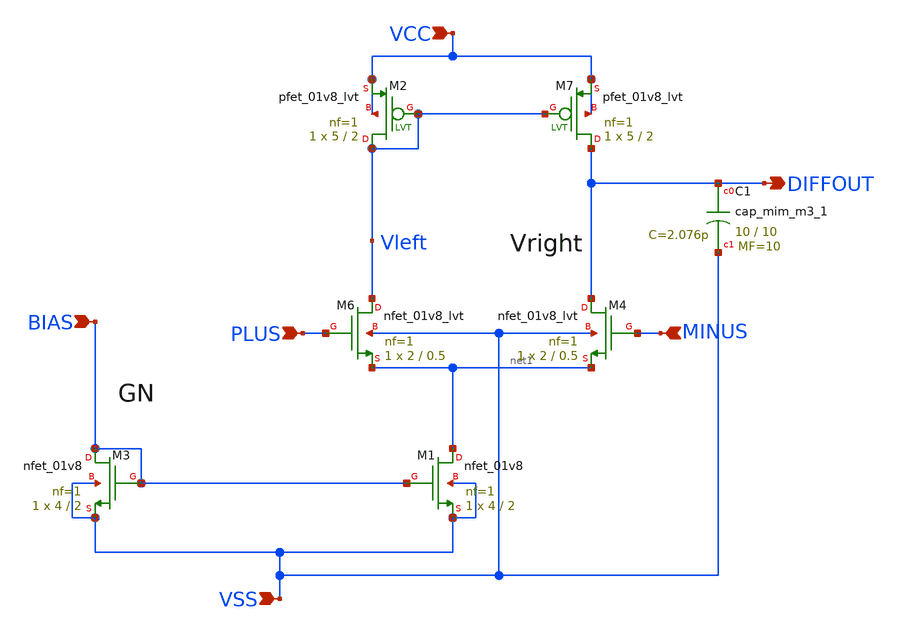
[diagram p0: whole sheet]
** sch_path: xschem/ota5t_1.sch
**.subckt ota5t_1 PLUS MINUS VCC VSS BIAS DIFFOUT
*.ipin PLUS
*.ipin MINUS
*.ipin VCC
*.ipin VSS
*.ipin BIAS
*.opin DIFFOUT
XM7 DIFFOUT Vleft VCC VCC sky130_fd_pr__pfet_01v8_lvt L=2 W=5 nf=1 ad='int((nf+1)/2) * W/nf * 0.29' as='int((nf+2)/2) * W/nf * 0.29'
+ pd='2*int((nf+1)/2) * (W/nf + 0.29)' ps='2*int((nf+2)/2) * (W/nf + 0.29)' nrd='0.29 / W' nrs='0.29 / W'
+ sa=0 sb=0 sd=0 mult=1 m=1
XM2 Vleft Vleft VCC VCC sky130_fd_pr__pfet_01v8_lvt L=2 W=5 nf=1 ad='int((nf+1)/2) * W/nf * 0.29' as='int((nf+2)/2) * W/nf * 0.29'
+ pd='2*int((nf+1)/2) * (W/nf + 0.29)' ps='2*int((nf+2)/2) * (W/nf + 0.29)' nrd='0.29 / W' nrs='0.29 / W'
+ sa=0 sb=0 sd=0 mult=1 m=1
XM6 Vleft PLUS net1 VSS sky130_fd_pr__nfet_01v8_lvt L=0.5 W=2 nf=1 ad='int((nf+1)/2) * W/nf * 0.29' as='int((nf+2)/2) * W/nf * 0.29'
+ pd='2*int((nf+1)/2) * (W/nf + 0.29)' ps='2*int((nf+2)/2) * (W/nf + 0.29)' nrd='0.29 / W' nrs='0.29 / W'
+ sa=0 sb=0 sd=0 mult=1 m=1
XM4 DIFFOUT MINUS net1 VSS sky130_fd_pr__nfet_01v8_lvt L=0.5 W=2 nf=1 ad='int((nf+1)/2) * W/nf * 0.29'
+ as='int((nf+2)/2) * W/nf * 0.29' pd='2*int((nf+1)/2) * (W/nf + 0.29)' ps='2*int((nf+2)/2) * (W/nf + 0.29)'
+ nrd='0.29 / W' nrs='0.29 / W' sa=0 sb=0 sd=0 mult=1 m=1
XM1 net1 BIAS VSS VSS sky130_fd_pr__nfet_01v8 L=2 W=4 nf=1 ad='int((nf+1)/2) * W/nf * 0.29' as='int((nf+2)/2) * W/nf * 0.29'
+ pd='2*int((nf+1)/2) * (W/nf + 0.29)' ps='2*int((nf+2)/2) * (W/nf + 0.29)' nrd='0.29 / W' nrs='0.29 / W'
+ sa=0 sb=0 sd=0 mult=1 m=1
XM3 BIAS BIAS VSS VSS sky130_fd_pr__nfet_01v8 L=2 W=4 nf=1 ad='int((nf+1)/2) * W/nf * 0.29' as='int((nf+2)/2) * W/nf * 0.29'
+ pd='2*int((nf+1)/2) * (W/nf + 0.29)' ps='2*int((nf+2)/2) * (W/nf + 0.29)' nrd='0.29 / W' nrs='0.29 / W'
+ sa=0 sb=0 sd=0 mult=1 m=1
XC1 DIFFOUT VSS sky130_fd_pr__cap_mim_m3_1 W=10 L=10 MF=10 m=10
**.ends
.end
